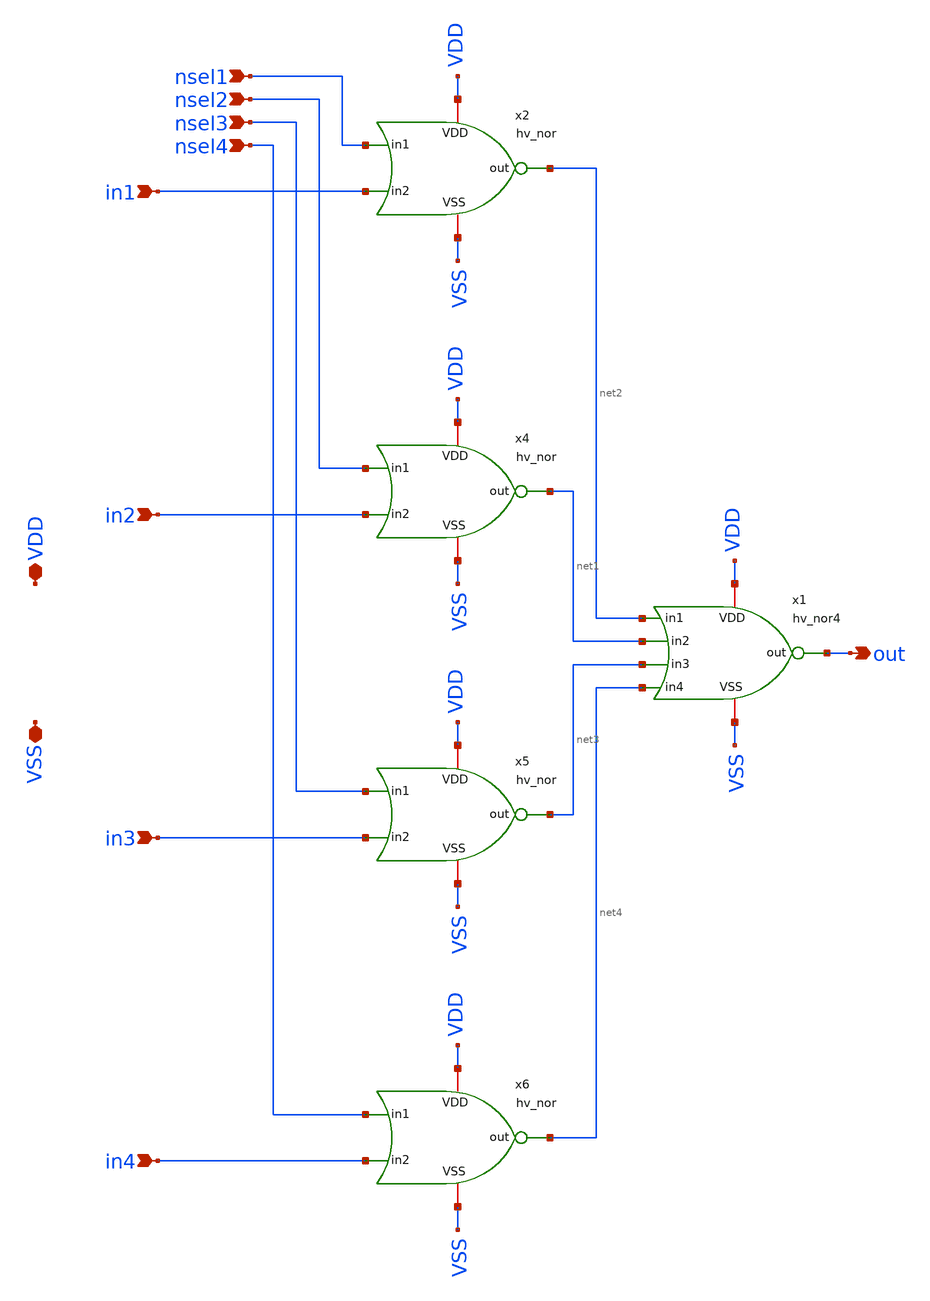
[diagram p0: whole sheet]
** sch_path: macros/heichips26_vcr/macros/switched_capacitor/schematic/xschem/hv_mux4.sch
**.subckt hv_mux4 in1 VDD VSS out in2 in3 in4 nsel1 nsel3 nsel2 nsel4
*.ipin in1
*.iopin VDD
*.iopin VSS
*.opin out
*.ipin in2
*.ipin in3
*.ipin in4
*.ipin nsel1
*.ipin nsel3
*.ipin nsel2
*.ipin nsel4
x1 VDD net2 out net1 VSS net3 net4 hv_nor4
x2 VDD nsel1 net2 in1 VSS hv_nor
x4 VDD nsel2 net1 in2 VSS hv_nor
x5 VDD nsel3 net3 in3 VSS hv_nor
x6 VDD nsel4 net4 in4 VSS hv_nor
**.ends

* expanding   symbol:  hv_nor4.sym # of pins=7
** sym_path: macros/heichips26_vcr/macros/switched_capacitor/schematic/xschem/hv_nor4.sym
** sch_path: macros/heichips26_vcr/macros/switched_capacitor/schematic/xschem/hv_nor4.sch
.subckt hv_nor4 VDD in1 out in2 VSS in3 in4
*.ipin in1
*.iopin VDD
*.iopin VSS
*.opin out
*.ipin in2
*.ipin in3
*.ipin in4
**** begin user architecture code


.param w   = 10u
.param ng  = 4
.param n_ng = ng
.param n_w = {3u*n_ng}
.param n_l = 0.45u
.param p_ng = ng
.param p_w = {10u*p_ng}
.param p_l = 0.4u


**** end user architecture code
XM2 out in3 VSS VSS sg13_hv_nmos w={n_w} l={n_l} ng={ng} m=1 mm_ok=1
XM3 net3 in4 VDD VDD sg13_hv_pmos w={p_w} l={p_l} ng={ng} m=1 mm_ok=1
XM1 out in4 VSS VSS sg13_hv_nmos w={n_w} l={n_l} ng={ng} m=1 mm_ok=1
XM4 out in1 net1 VDD sg13_hv_pmos w={p_w} l={p_l} ng={ng} m=1 mm_ok=1
XM5 out in2 VSS VSS sg13_hv_nmos w={n_w} l={n_l} ng={ng} m=1 mm_ok=1
XM6 out in1 VSS VSS sg13_hv_nmos w={n_w} l={n_l} ng={ng} m=1 mm_ok=1
XM7 net1 in2 net2 VDD sg13_hv_pmos w={p_w} l={p_l} ng={ng} m=1 mm_ok=1
XM8 net2 in3 net3 VDD sg13_hv_pmos w={p_w} l={p_l} ng={ng} m=1 mm_ok=1
.ends


* expanding   symbol:  hv_nor.sym # of pins=5
** sym_path: macros/heichips26_vcr/macros/switched_capacitor/schematic/xschem/hv_nor.sym
** sch_path: macros/heichips26_vcr/macros/switched_capacitor/schematic/xschem/hv_nor.sch
.subckt hv_nor VDD in1 out in2 VSS
*.ipin in1
*.iopin VDD
*.iopin VSS
*.opin out
*.ipin in2
**** begin user architecture code


.param w   = 10u
.param ng  = 4
.param n_ng = ng
.param n_w = {3u*n_ng}
.param n_l = 0.45u
.param p_ng = ng
.param p_w = {10u*p_ng}
.param p_l = 0.4u


**** end user architecture code
XM2 out in1 VSS VSS sg13_hv_nmos w={n_w} l={n_l} ng={ng} m=1 mm_ok=1
XM3 net1 in2 VDD VDD sg13_hv_pmos w={p_w} l={p_l} ng={ng} m=1 mm_ok=1
XM1 out in2 VSS VSS sg13_hv_nmos w={n_w} l={n_l} ng={ng} m=1 mm_ok=1
XM4 out in1 net1 VDD sg13_hv_pmos w={p_w} l={p_l} ng={ng} m=1 mm_ok=1
.ends

.end
